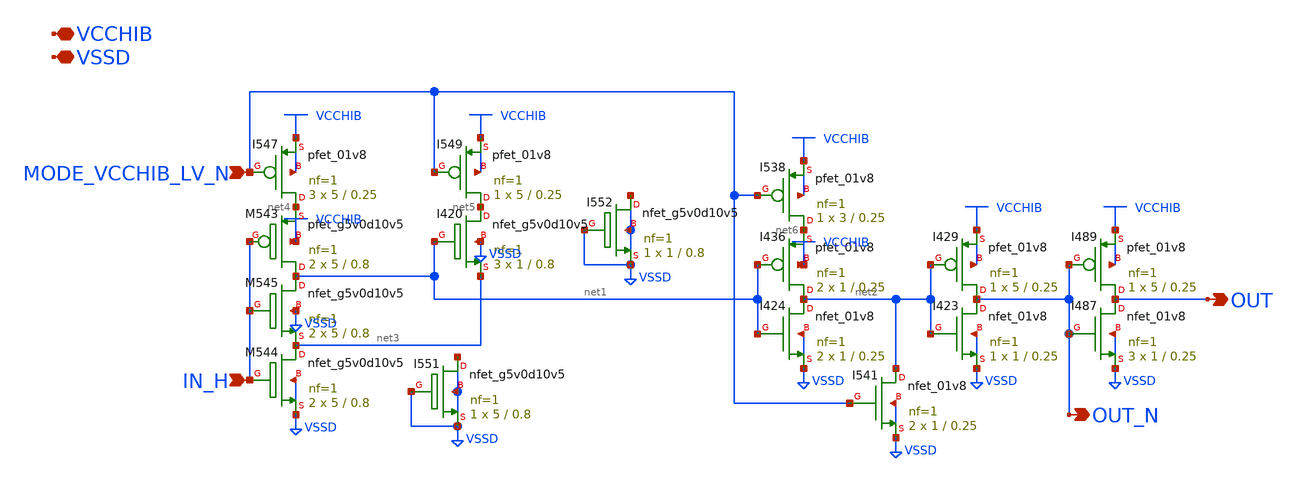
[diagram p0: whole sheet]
** sch_path: gpiov2_vcchib_in_buf.sch
* Copyright 2023 David Mitchell Bailey
* Licensed under the Apache License, Version 2.0 (the "License");
* you may not use this file except in compliance with the License.
* You may obtain a copy of the License at
* https://www.apache.org/licenses/LICENSE-2.0
* Unless required by applicable law or agreed to in writing, software
* distributed under the License is distributed on an "AS IS" BASIS,
* WITHOUT WARRANTIES OR CONDITIONS OF ANY KIND, either express or implied.
* See the License for the specific language governing permissions and
* limitations under the License.
**.subckt gpiov2_vcchib_in_buf IN_H VCCHIB VSSD OUT MODE_VCCHIB_LV_N OUT_N
*.ipin IN_H
*.iopin VCCHIB
*.iopin VSSD
*.opin OUT
*.ipin MODE_VCCHIB_LV_N
*.opin OUT_N
XM544 net3 IN_H VSSD VSSD sky130_fd_pr__nfet_g5v0d10v5 L=0.8 W=5 nf=1 ad='int((nf+1)/2) * W/nf * 0.29'
+ as='int((nf+2)/2) * W/nf * 0.29' pd='2*int((nf+1)/2) * (W/nf + 0.29)' ps='2*int((nf+2)/2) * (W/nf + 0.29)'
+ nrd='0.29 / W' nrs='0.29 / W' sa=0 sb=0 sd=0 mult=2 m=2
XM545 net1 IN_H net3 VSSD sky130_fd_pr__nfet_g5v0d10v5 L=0.8 W=5 nf=1 ad='int((nf+1)/2) * W/nf * 0.29'
+ as='int((nf+2)/2) * W/nf * 0.29' pd='2*int((nf+1)/2) * (W/nf + 0.29)' ps='2*int((nf+2)/2) * (W/nf + 0.29)'
+ nrd='0.29 / W' nrs='0.29 / W' sa=0 sb=0 sd=0 mult=2 m=2
XM543 net1 IN_H net4 VCCHIB sky130_fd_pr__pfet_g5v0d10v5 L=0.8 W=5 nf=1 ad='int((nf+1)/2) * W/nf * 0.29'
+ as='int((nf+2)/2) * W/nf * 0.29' pd='2*int((nf+1)/2) * (W/nf + 0.29)' ps='2*int((nf+2)/2) * (W/nf + 0.29)'
+ nrd='0.29 / W' nrs='0.29 / W' sa=0 sb=0 sd=0 mult=2 m=2
XI547 net4 MODE_VCCHIB_LV_N VCCHIB VCCHIB sky130_fd_pr__pfet_01v8 L=0.25 W=5 nf=1 ad='int((nf+1)/2) * W/nf * 0.29'
+ as='int((nf+2)/2) * W/nf * 0.29' pd='2*int((nf+1)/2) * (W/nf + 0.29)' ps='2*int((nf+2)/2) * (W/nf + 0.29)'
+ nrd='0.29 / W' nrs='0.29 / W' sa=0 sb=0 sd=0 mult=3 m=3
XI549 net5 MODE_VCCHIB_LV_N VCCHIB VCCHIB sky130_fd_pr__pfet_01v8 L=0.25 W=5 nf=1 ad='int((nf+1)/2) * W/nf * 0.29'
+ as='int((nf+2)/2) * W/nf * 0.29' pd='2*int((nf+1)/2) * (W/nf + 0.29)' ps='2*int((nf+2)/2) * (W/nf + 0.29)'
+ nrd='0.29 / W' nrs='0.29 / W' sa=0 sb=0 sd=0 mult=1 m=1
XI420 net5 net1 net3 VSSD sky130_fd_pr__nfet_g5v0d10v5 L=0.8 W=1 nf=1 ad='int((nf+1)/2) * W/nf * 0.29'
+ as='int((nf+2)/2) * W/nf * 0.29' pd='2*int((nf+1)/2) * (W/nf + 0.29)' ps='2*int((nf+2)/2) * (W/nf + 0.29)'
+ nrd='0.29 / W' nrs='0.29 / W' sa=0 sb=0 sd=0 mult=3 m=3
XI538 net6 MODE_VCCHIB_LV_N VCCHIB VCCHIB sky130_fd_pr__pfet_01v8 L=0.25 W=3 nf=1 ad='int((nf+1)/2) * W/nf * 0.29'
+ as='int((nf+2)/2) * W/nf * 0.29' pd='2*int((nf+1)/2) * (W/nf + 0.29)' ps='2*int((nf+2)/2) * (W/nf + 0.29)'
+ nrd='0.29 / W' nrs='0.29 / W' sa=0 sb=0 sd=0 mult=1 m=1
XI436 net2 net1 net6 VCCHIB sky130_fd_pr__pfet_01v8 L=0.25 W=1 nf=1 ad='int((nf+1)/2) * W/nf * 0.29'
+ as='int((nf+2)/2) * W/nf * 0.29' pd='2*int((nf+1)/2) * (W/nf + 0.29)' ps='2*int((nf+2)/2) * (W/nf + 0.29)'
+ nrd='0.29 / W' nrs='0.29 / W' sa=0 sb=0 sd=0 mult=2 m=2
XI424 net2 net1 VSSD VSSD sky130_fd_pr__nfet_01v8 L=0.25 W=1 nf=1 ad='int((nf+1)/2) * W/nf * 0.29' as='int((nf+2)/2) * W/nf * 0.29'
+ pd='2*int((nf+1)/2) * (W/nf + 0.29)' ps='2*int((nf+2)/2) * (W/nf + 0.29)' nrd='0.29 / W' nrs='0.29 / W'
+ sa=0 sb=0 sd=0 mult=2 m=2
XI541 net2 MODE_VCCHIB_LV_N VSSD VSSD sky130_fd_pr__nfet_01v8 L=0.25 W=1 nf=1 ad='int((nf+1)/2) * W/nf * 0.29'
+ as='int((nf+2)/2) * W/nf * 0.29' pd='2*int((nf+1)/2) * (W/nf + 0.29)' ps='2*int((nf+2)/2) * (W/nf + 0.29)'
+ nrd='0.29 / W' nrs='0.29 / W' sa=0 sb=0 sd=0 mult=2 m=2
XI429 OUT_N net2 VCCHIB VCCHIB sky130_fd_pr__pfet_01v8 L=0.25 W=5 nf=1 ad='int((nf+1)/2) * W/nf * 0.29'
+ as='int((nf+2)/2) * W/nf * 0.29' pd='2*int((nf+1)/2) * (W/nf + 0.29)' ps='2*int((nf+2)/2) * (W/nf + 0.29)'
+ nrd='0.29 / W' nrs='0.29 / W' sa=0 sb=0 sd=0 mult=1 m=1
XI423 OUT_N net2 VSSD VSSD sky130_fd_pr__nfet_01v8 L=0.25 W=1 nf=1 ad='int((nf+1)/2) * W/nf * 0.29' as='int((nf+2)/2) * W/nf * 0.29'
+ pd='2*int((nf+1)/2) * (W/nf + 0.29)' ps='2*int((nf+2)/2) * (W/nf + 0.29)' nrd='0.29 / W' nrs='0.29 / W'
+ sa=0 sb=0 sd=0 mult=1 m=1
XI489 OUT OUT_N VCCHIB VCCHIB sky130_fd_pr__pfet_01v8 L=0.25 W=5 nf=1 ad='int((nf+1)/2) * W/nf * 0.29'
+ as='int((nf+2)/2) * W/nf * 0.29' pd='2*int((nf+1)/2) * (W/nf + 0.29)' ps='2*int((nf+2)/2) * (W/nf + 0.29)'
+ nrd='0.29 / W' nrs='0.29 / W' sa=0 sb=0 sd=0 mult=1 m=1
XI487 OUT OUT_N VSSD VSSD sky130_fd_pr__nfet_01v8 L=0.25 W=1 nf=1 ad='int((nf+1)/2) * W/nf * 0.29' as='int((nf+2)/2) * W/nf * 0.29'
+ pd='2*int((nf+1)/2) * (W/nf + 0.29)' ps='2*int((nf+2)/2) * (W/nf + 0.29)' nrd='0.29 / W' nrs='0.29 / W'
+ sa=0 sb=0 sd=0 mult=3 m=3
XI551 VSSD VSSD VSSD VSSD sky130_fd_pr__nfet_g5v0d10v5 L=0.8 W=5 nf=1 ad='int((nf+1)/2) * W/nf * 0.29'
+ as='int((nf+2)/2) * W/nf * 0.29' pd='2*int((nf+1)/2) * (W/nf + 0.29)' ps='2*int((nf+2)/2) * (W/nf + 0.29)'
+ nrd='0.29 / W' nrs='0.29 / W' sa=0 sb=0 sd=0 mult=1 m=1
XI552 VSSD VSSD VSSD VSSD sky130_fd_pr__nfet_g5v0d10v5 L=0.8 W=1 nf=1 ad='int((nf+1)/2) * W/nf * 0.29'
+ as='int((nf+2)/2) * W/nf * 0.29' pd='2*int((nf+1)/2) * (W/nf + 0.29)' ps='2*int((nf+2)/2) * (W/nf + 0.29)'
+ nrd='0.29 / W' nrs='0.29 / W' sa=0 sb=0 sd=0 mult=1 m=1
**.ends
.end
